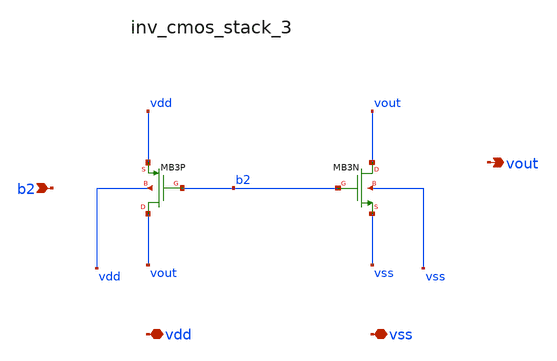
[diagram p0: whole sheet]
** sch_path: analog-db/raw/cmp_001_hyst_diffpair/hier/blocks/inv_cmos_stack_3.sch
**.subckt inv_cmos_stack_3 b2 vdd vss vout
*.ipin b2
*.iopin vdd
*.iopin vss
*.opin vout
XMB3N vout b2 vss vss sg13_lv_nmos w=x_dut_xmb3n_w l=x_dut_xmb3n_l ng=1 m=x_dut_xmb3n_m
XMB3P vout b2 vdd vdd sg13_lv_pmos w=x_dut_xmb3p_w l=x_dut_xmb3p_l ng=1 m=x_dut_xmb3p_m
**.ends
.end
